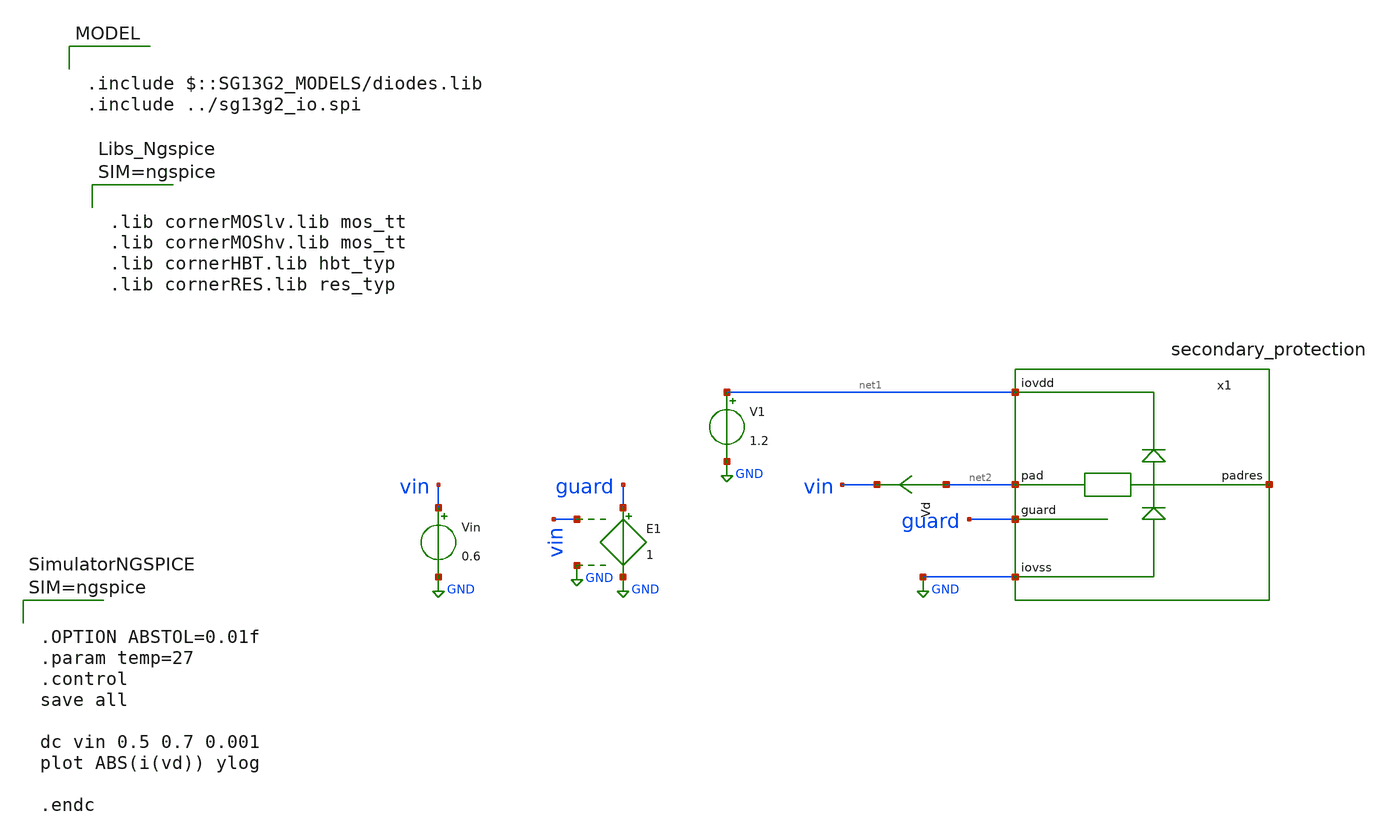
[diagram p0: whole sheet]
** sch_path: trident_test_structures/design_data/xschem/IOPadAnalog_submodules/secondary_protection_tb.sch
**.subckt secondary_protection_tb
Vd net2 vin 0
.save i(vd)
Vin vin GND 0.6
V1 net1 GND 1.2
E1 guard GND vin GND 1
x1 net1 net2 net3 guard GND secondary_protection
**** begin user architecture code



.lib cornerMOSlv.lib mos_tt
.lib cornerMOShv.lib mos_tt
.lib cornerHBT.lib hbt_typ
.lib cornerRES.lib res_typ







.OPTION ABSTOL=0.01f
.param temp=27
.control
save all

dc vin 0.5 0.7 0.001
plot ABS(i(vd)) ylog

.endc




.include $::SG13G2_MODELS/diodes.lib
.include ../sg13g2_io.spi

**** end user architecture code
**.ends

* expanding   symbol:  secondary_protection.sym # of pins=5
** sym_path: trident_test_structures/design_data/xschem/IOPadAnalog_submodules/secondary_protection.sym
** sch_path: trident_test_structures/design_data/xschem/IOPadAnalog_submodules/secondary_protection.sch
.subckt secondary_protection iovdd pad padres pad_guard iovss
*.iopin iovdd
*.iopin pad
*.iopin pad_guard
*.iopin iovss
*.iopin padres
x1 iovdd iovss pad padres sg13g2_SecondaryProtection
.ends

.GLOBAL GND
.end
